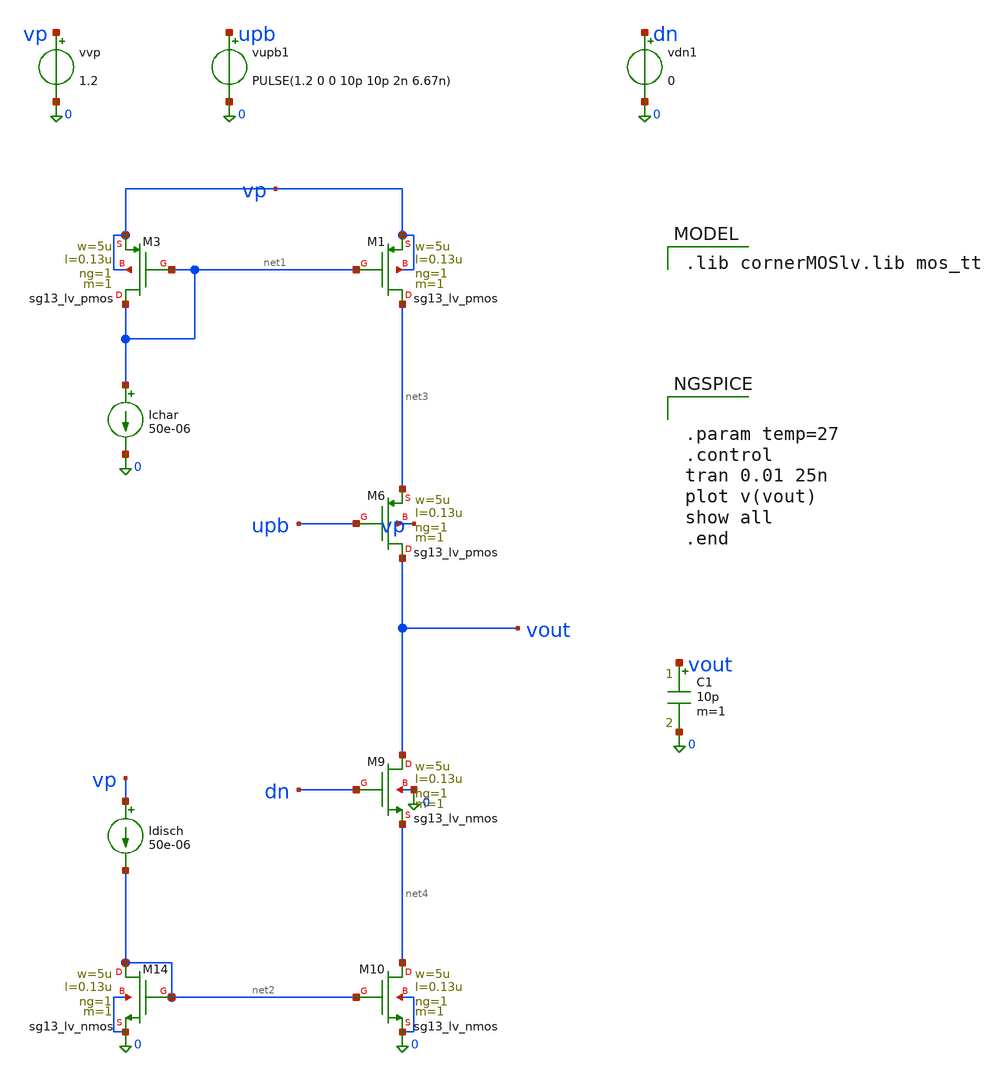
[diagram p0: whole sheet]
** sch_path: schematics/charge_pump/old_sch/cp_v3_tb.sch
**.subckt cp_v3_tb
XM3 net1 net1 vp vp sg13_lv_pmos w=5u l=0.13u ng=1 m=1 mm_ok=1
XM1 net3 net1 vp vp sg13_lv_pmos w=5u l=0.13u ng=1 m=1 mm_ok=1
XM6 vout upb net3 vp sg13_lv_pmos w=5u l=0.13u ng=1 m=1 mm_ok=1
XM9 vout dn net4 0 sg13_lv_nmos w=5u l=0.13u ng=1 m=1 mm_ok=1
XM10 net4 net2 0 0 sg13_lv_nmos w=5u l=0.13u ng=1 m=1 mm_ok=1
XM14 net2 net2 0 0 sg13_lv_nmos w=5u l=0.13u ng=1 m=1 mm_ok=1
Ichar net1 0 50e-06
Idisch vp net2 50e-06
vvp vp 0 1.2
C1 vout 0 10p m=1
vupb1 upb 0 PULSE(1.2 0 0 10p 10p 2n 6.67n)
vdn1 dn 0 0
**** begin user architecture code
 .lib cornerMOSlv.lib mos_tt



.param temp=27
.control
tran 0.01 25n
plot v(vout)
show all
.end


**** end user architecture code
**.ends
.end
